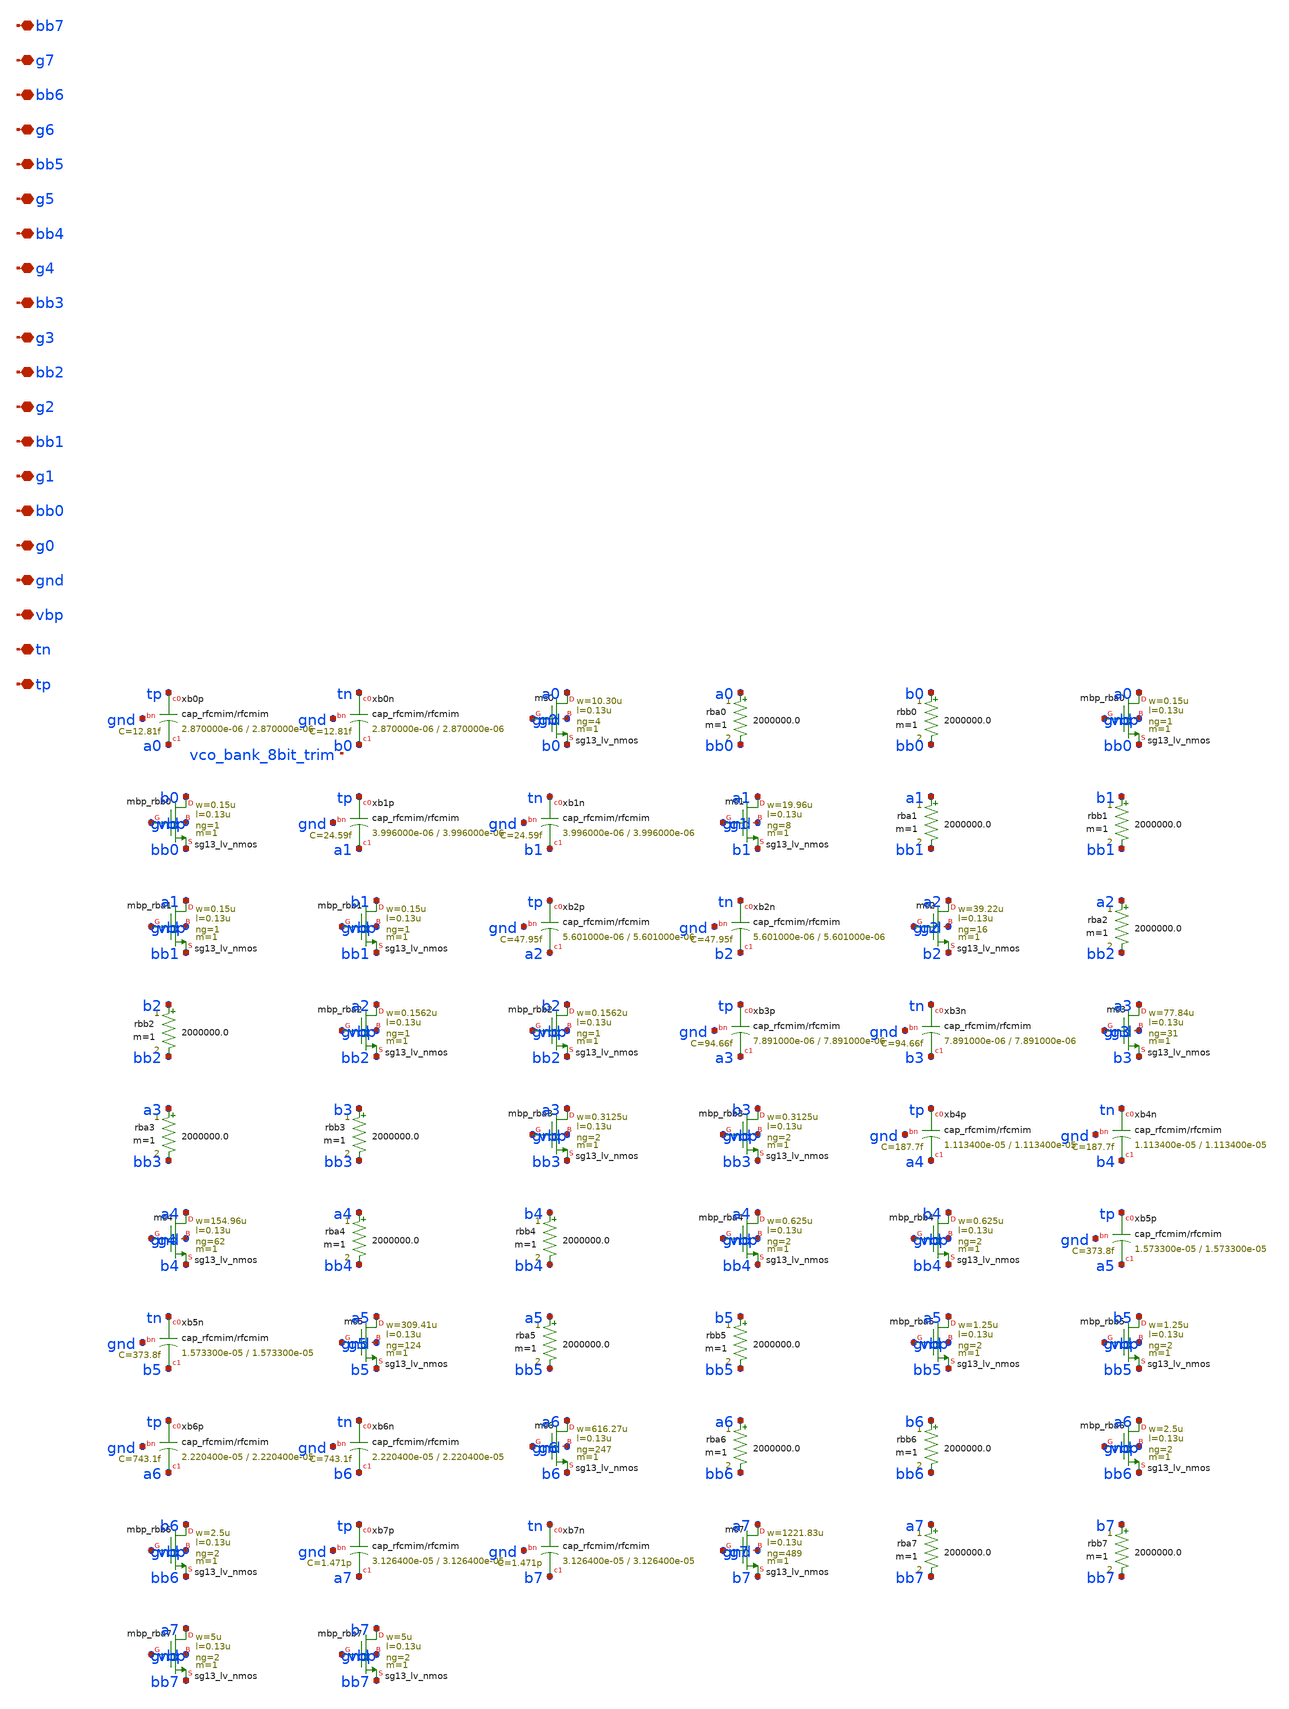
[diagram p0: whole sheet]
** sch_path: analog/vco/sch/vco_bank.sch
**.subckt vco_bank tp tn vbp gnd g0 bb0 g1 bb1 g2 bb2 g3 bb3 g4 bb4 g5 bb5 g6 bb6 g7 bb7
*.iopin tp
*.iopin tn
*.iopin vbp
*.iopin gnd
*.iopin g0
*.iopin bb0
*.iopin g1
*.iopin bb1
*.iopin g2
*.iopin bb2
*.iopin g3
*.iopin bb3
*.iopin g4
*.iopin bb4
*.iopin g5
*.iopin bb5
*.iopin g6
*.iopin bb6
*.iopin g7
*.iopin bb7
Xxb0p tp a0 gnd cap_rfcmim w=2.870000e-06 l=2.870000e-06 wfeed=5.0e-6 m=1 mm_ok=1
Xxb0n tn b0 gnd cap_rfcmim w=2.870000e-06 l=2.870000e-06 wfeed=5.0e-6 m=1 mm_ok=1
Xms0 a0 g0 b0 gnd sg13_lv_nmos w=10.30u l=0.13u ng=4 m=1 mm_ok=1
rba0 a0 bb0 2000000.0 m=1
rbb0 b0 bb0 2000000.0 m=1
Xmbp_rba0 a0 vbp bb0 gnd sg13_lv_nmos w=0.15u l=0.13u ng=1 m=1 mm_ok=1
Xmbp_rbb0 b0 vbp bb0 gnd sg13_lv_nmos w=0.15u l=0.13u ng=1 m=1 mm_ok=1
Xxb1p tp a1 gnd cap_rfcmim w=3.996000e-06 l=3.996000e-06 wfeed=5.0e-6 m=1 mm_ok=1
Xxb1n tn b1 gnd cap_rfcmim w=3.996000e-06 l=3.996000e-06 wfeed=5.0e-6 m=1 mm_ok=1
Xms1 a1 g1 b1 gnd sg13_lv_nmos w=19.96u l=0.13u ng=8 m=1 mm_ok=1
rba1 a1 bb1 2000000.0 m=1
rbb1 b1 bb1 2000000.0 m=1
Xmbp_rba1 a1 vbp bb1 gnd sg13_lv_nmos w=0.15u l=0.13u ng=1 m=1 mm_ok=1
Xmbp_rbb1 b1 vbp bb1 gnd sg13_lv_nmos w=0.15u l=0.13u ng=1 m=1 mm_ok=1
Xxb2p tp a2 gnd cap_rfcmim w=5.601000e-06 l=5.601000e-06 wfeed=5.0e-6 m=1 mm_ok=1
Xxb2n tn b2 gnd cap_rfcmim w=5.601000e-06 l=5.601000e-06 wfeed=5.0e-6 m=1 mm_ok=1
Xms2 a2 g2 b2 gnd sg13_lv_nmos w=39.22u l=0.13u ng=16 m=1 mm_ok=1
rba2 a2 bb2 2000000.0 m=1
rbb2 b2 bb2 2000000.0 m=1
Xmbp_rba2 a2 vbp bb2 gnd sg13_lv_nmos w=0.1562u l=0.13u ng=1 m=1 mm_ok=1
Xmbp_rbb2 b2 vbp bb2 gnd sg13_lv_nmos w=0.1562u l=0.13u ng=1 m=1 mm_ok=1
Xxb3p tp a3 gnd cap_rfcmim w=7.891000e-06 l=7.891000e-06 wfeed=5.0e-6 m=1 mm_ok=1
Xxb3n tn b3 gnd cap_rfcmim w=7.891000e-06 l=7.891000e-06 wfeed=5.0e-6 m=1 mm_ok=1
Xms3 a3 g3 b3 gnd sg13_lv_nmos w=77.84u l=0.13u ng=31 m=1 mm_ok=1
rba3 a3 bb3 2000000.0 m=1
rbb3 b3 bb3 2000000.0 m=1
Xmbp_rba3 a3 vbp bb3 gnd sg13_lv_nmos w=0.3125u l=0.13u ng=2 m=1 mm_ok=1
Xmbp_rbb3 b3 vbp bb3 gnd sg13_lv_nmos w=0.3125u l=0.13u ng=2 m=1 mm_ok=1
Xxb4p tp a4 gnd cap_rfcmim w=1.113400e-05 l=1.113400e-05 wfeed=5.0e-6 m=1 mm_ok=1
Xxb4n tn b4 gnd cap_rfcmim w=1.113400e-05 l=1.113400e-05 wfeed=5.0e-6 m=1 mm_ok=1
Xms4 a4 g4 b4 gnd sg13_lv_nmos w=154.96u l=0.13u ng=62 m=1 mm_ok=1
rba4 a4 bb4 2000000.0 m=1
rbb4 b4 bb4 2000000.0 m=1
Xmbp_rba4 a4 vbp bb4 gnd sg13_lv_nmos w=0.625u l=0.13u ng=2 m=1 mm_ok=1
Xmbp_rbb4 b4 vbp bb4 gnd sg13_lv_nmos w=0.625u l=0.13u ng=2 m=1 mm_ok=1
Xxb5p tp a5 gnd cap_rfcmim w=1.573300e-05 l=1.573300e-05 wfeed=5.0e-6 m=1 mm_ok=1
Xxb5n tn b5 gnd cap_rfcmim w=1.573300e-05 l=1.573300e-05 wfeed=5.0e-6 m=1 mm_ok=1
Xms5 a5 g5 b5 gnd sg13_lv_nmos w=309.41u l=0.13u ng=124 m=1 mm_ok=1
rba5 a5 bb5 2000000.0 m=1
rbb5 b5 bb5 2000000.0 m=1
Xmbp_rba5 a5 vbp bb5 gnd sg13_lv_nmos w=1.25u l=0.13u ng=2 m=1 mm_ok=1
Xmbp_rbb5 b5 vbp bb5 gnd sg13_lv_nmos w=1.25u l=0.13u ng=2 m=1 mm_ok=1
Xxb6p tp a6 gnd cap_rfcmim w=2.220400e-05 l=2.220400e-05 wfeed=5.0e-6 m=1 mm_ok=1
Xxb6n tn b6 gnd cap_rfcmim w=2.220400e-05 l=2.220400e-05 wfeed=5.0e-6 m=1 mm_ok=1
Xms6 a6 g6 b6 gnd sg13_lv_nmos w=616.27u l=0.13u ng=247 m=1 mm_ok=1
rba6 a6 bb6 2000000.0 m=1
rbb6 b6 bb6 2000000.0 m=1
Xmbp_rba6 a6 vbp bb6 gnd sg13_lv_nmos w=2.5u l=0.13u ng=2 m=1 mm_ok=1
Xmbp_rbb6 b6 vbp bb6 gnd sg13_lv_nmos w=2.5u l=0.13u ng=2 m=1 mm_ok=1
Xxb7p tp a7 gnd cap_rfcmim w=3.126400e-05 l=3.126400e-05 wfeed=5.0e-6 m=1 mm_ok=1
Xxb7n tn b7 gnd cap_rfcmim w=3.126400e-05 l=3.126400e-05 wfeed=5.0e-6 m=1 mm_ok=1
Xms7 a7 g7 b7 gnd sg13_lv_nmos w=1221.83u l=0.13u ng=489 m=1 mm_ok=1
rba7 a7 bb7 2000000.0 m=1
rbb7 b7 bb7 2000000.0 m=1
Xmbp_rba7 a7 vbp bb7 gnd sg13_lv_nmos w=5u l=0.13u ng=2 m=1 mm_ok=1
Xmbp_rbb7 b7 vbp bb7 gnd sg13_lv_nmos w=5u l=0.13u ng=2 m=1 mm_ok=1
**.ends
.end
